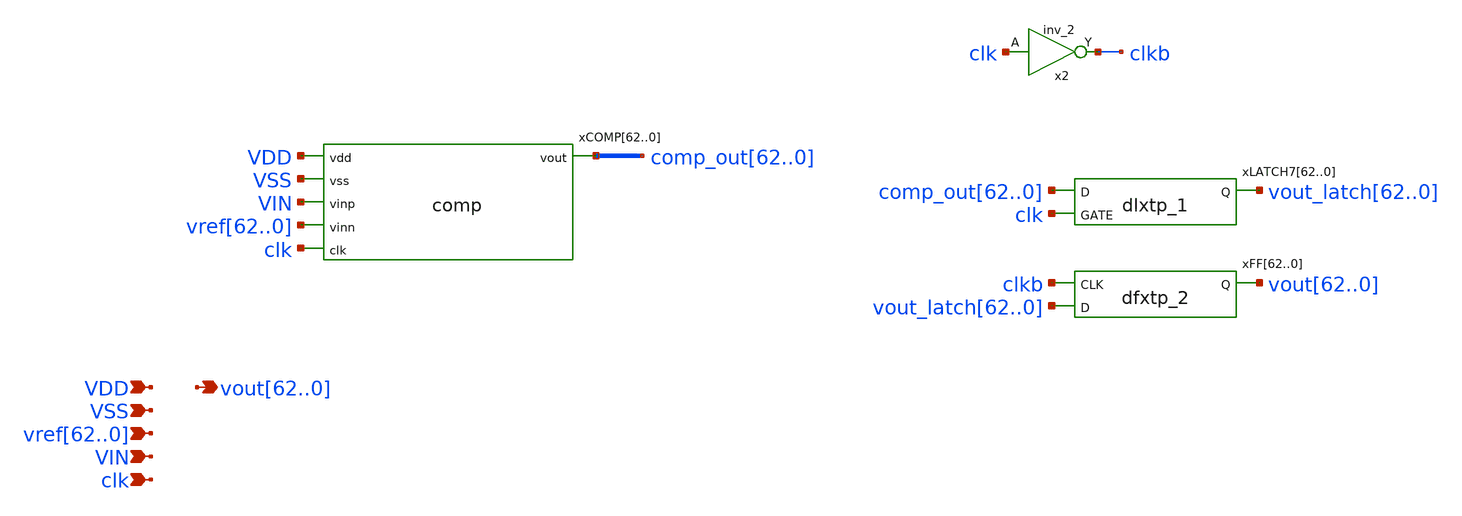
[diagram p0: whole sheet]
** sch_path: schematics/comp_top.sch
**.subckt comp_top
*+ vout62,vout61,vout60,vout59,vout58,vout57,vout56,vout55,vout54,vout53,vout52,vout51,vout50,vout49,vout48,vout47,vout46,vout45,vout44,vout43,vout42,vout41,vout40,vout39,vout38,vout37,vout36,vout35,vout34,vout33,vout32,vout31,vout30,vout29,vout28,vout27,vout26,vout25,vout24,vout23,vout22,vout21,vout20,vout19,vout18,vout17,vout16,vout15,vout14,vout13,vout12,vout11,vout10,vout9,vout8,vout7,vout6,vout5,vout4,vout3,vout2,vout1,vout0 VDD VSS
*+ vref62,vref61,vref60,vref59,vref58,vref57,vref56,vref55,vref54,vref53,vref52,vref51,vref50,vref49,vref48,vref47,vref46,vref45,vref44,vref43,vref42,vref41,vref40,vref39,vref38,vref37,vref36,vref35,vref34,vref33,vref32,vref31,vref30,vref29,vref28,vref27,vref26,vref25,vref24,vref23,vref22,vref21,vref20,vref19,vref18,vref17,vref16,vref15,vref14,vref13,vref12,vref11,vref10,vref9,vref8,vref7,vref6,vref5,vref4,vref3,vref2,vref1,vref0 VIN clk
*.opin
*+ vout62,vout61,vout60,vout59,vout58,vout57,vout56,vout55,vout54,vout53,vout52,vout51,vout50,vout49,vout48,vout47,vout46,vout45,vout44,vout43,vout42,vout41,vout40,vout39,vout38,vout37,vout36,vout35,vout34,vout33,vout32,vout31,vout30,vout29,vout28,vout27,vout26,vout25,vout24,vout23,vout22,vout21,vout20,vout19,vout18,vout17,vout16,vout15,vout14,vout13,vout12,vout11,vout10,vout9,vout8,vout7,vout6,vout5,vout4,vout3,vout2,vout1,vout0
*.ipin VDD
*.ipin VSS
*.ipin
*+ vref62,vref61,vref60,vref59,vref58,vref57,vref56,vref55,vref54,vref53,vref52,vref51,vref50,vref49,vref48,vref47,vref46,vref45,vref44,vref43,vref42,vref41,vref40,vref39,vref38,vref37,vref36,vref35,vref34,vref33,vref32,vref31,vref30,vref29,vref28,vref27,vref26,vref25,vref24,vref23,vref22,vref21,vref20,vref19,vref18,vref17,vref16,vref15,vref14,vref13,vref12,vref11,vref10,vref9,vref8,vref7,vref6,vref5,vref4,vref3,vref2,vref1,vref0
*.ipin VIN
*.ipin clk
xCOMP62 comp_out62 VDD VSS VIN vref62 clk comp
xCOMP61 comp_out61 VDD VSS VIN vref61 clk comp
xCOMP60 comp_out60 VDD VSS VIN vref60 clk comp
xCOMP59 comp_out59 VDD VSS VIN vref59 clk comp
xCOMP58 comp_out58 VDD VSS VIN vref58 clk comp
xCOMP57 comp_out57 VDD VSS VIN vref57 clk comp
xCOMP56 comp_out56 VDD VSS VIN vref56 clk comp
xCOMP55 comp_out55 VDD VSS VIN vref55 clk comp
xCOMP54 comp_out54 VDD VSS VIN vref54 clk comp
xCOMP53 comp_out53 VDD VSS VIN vref53 clk comp
xCOMP52 comp_out52 VDD VSS VIN vref52 clk comp
xCOMP51 comp_out51 VDD VSS VIN vref51 clk comp
xCOMP50 comp_out50 VDD VSS VIN vref50 clk comp
xCOMP49 comp_out49 VDD VSS VIN vref49 clk comp
xCOMP48 comp_out48 VDD VSS VIN vref48 clk comp
xCOMP47 comp_out47 VDD VSS VIN vref47 clk comp
xCOMP46 comp_out46 VDD VSS VIN vref46 clk comp
xCOMP45 comp_out45 VDD VSS VIN vref45 clk comp
xCOMP44 comp_out44 VDD VSS VIN vref44 clk comp
xCOMP43 comp_out43 VDD VSS VIN vref43 clk comp
xCOMP42 comp_out42 VDD VSS VIN vref42 clk comp
xCOMP41 comp_out41 VDD VSS VIN vref41 clk comp
xCOMP40 comp_out40 VDD VSS VIN vref40 clk comp
xCOMP39 comp_out39 VDD VSS VIN vref39 clk comp
xCOMP38 comp_out38 VDD VSS VIN vref38 clk comp
xCOMP37 comp_out37 VDD VSS VIN vref37 clk comp
xCOMP36 comp_out36 VDD VSS VIN vref36 clk comp
xCOMP35 comp_out35 VDD VSS VIN vref35 clk comp
xCOMP34 comp_out34 VDD VSS VIN vref34 clk comp
xCOMP33 comp_out33 VDD VSS VIN vref33 clk comp
xCOMP32 comp_out32 VDD VSS VIN vref32 clk comp
xCOMP31 comp_out31 VDD VSS VIN vref31 clk comp
xCOMP30 comp_out30 VDD VSS VIN vref30 clk comp
xCOMP29 comp_out29 VDD VSS VIN vref29 clk comp
xCOMP28 comp_out28 VDD VSS VIN vref28 clk comp
xCOMP27 comp_out27 VDD VSS VIN vref27 clk comp
xCOMP26 comp_out26 VDD VSS VIN vref26 clk comp
xCOMP25 comp_out25 VDD VSS VIN vref25 clk comp
xCOMP24 comp_out24 VDD VSS VIN vref24 clk comp
xCOMP23 comp_out23 VDD VSS VIN vref23 clk comp
xCOMP22 comp_out22 VDD VSS VIN vref22 clk comp
xCOMP21 comp_out21 VDD VSS VIN vref21 clk comp
xCOMP20 comp_out20 VDD VSS VIN vref20 clk comp
xCOMP19 comp_out19 VDD VSS VIN vref19 clk comp
xCOMP18 comp_out18 VDD VSS VIN vref18 clk comp
xCOMP17 comp_out17 VDD VSS VIN vref17 clk comp
xCOMP16 comp_out16 VDD VSS VIN vref16 clk comp
xCOMP15 comp_out15 VDD VSS VIN vref15 clk comp
xCOMP14 comp_out14 VDD VSS VIN vref14 clk comp
xCOMP13 comp_out13 VDD VSS VIN vref13 clk comp
xCOMP12 comp_out12 VDD VSS VIN vref12 clk comp
xCOMP11 comp_out11 VDD VSS VIN vref11 clk comp
xCOMP10 comp_out10 VDD VSS VIN vref10 clk comp
xCOMP9 comp_out9 VDD VSS VIN vref9 clk comp
xCOMP8 comp_out8 VDD VSS VIN vref8 clk comp
xCOMP7 comp_out7 VDD VSS VIN vref7 clk comp
xCOMP6 comp_out6 VDD VSS VIN vref6 clk comp
xCOMP5 comp_out5 VDD VSS VIN vref5 clk comp
xCOMP4 comp_out4 VDD VSS VIN vref4 clk comp
xCOMP3 comp_out3 VDD VSS VIN vref3 clk comp
xCOMP2 comp_out2 VDD VSS VIN vref2 clk comp
xCOMP1 comp_out1 VDD VSS VIN vref1 clk comp
xCOMP0 comp_out0 VDD VSS VIN vref0 clk comp
x2 clk vss vss vdd vdd clkb sky130_fd_sc_hd__inv_2
xLATCH762 comp_out62 clk vss vss vdd vdd vout_latch62 sky130_fd_sc_hd__dlxtp_1
xLATCH761 comp_out61 clk vss vss vdd vdd vout_latch61 sky130_fd_sc_hd__dlxtp_1
xLATCH760 comp_out60 clk vss vss vdd vdd vout_latch60 sky130_fd_sc_hd__dlxtp_1
xLATCH759 comp_out59 clk vss vss vdd vdd vout_latch59 sky130_fd_sc_hd__dlxtp_1
xLATCH758 comp_out58 clk vss vss vdd vdd vout_latch58 sky130_fd_sc_hd__dlxtp_1
xLATCH757 comp_out57 clk vss vss vdd vdd vout_latch57 sky130_fd_sc_hd__dlxtp_1
xLATCH756 comp_out56 clk vss vss vdd vdd vout_latch56 sky130_fd_sc_hd__dlxtp_1
xLATCH755 comp_out55 clk vss vss vdd vdd vout_latch55 sky130_fd_sc_hd__dlxtp_1
xLATCH754 comp_out54 clk vss vss vdd vdd vout_latch54 sky130_fd_sc_hd__dlxtp_1
xLATCH753 comp_out53 clk vss vss vdd vdd vout_latch53 sky130_fd_sc_hd__dlxtp_1
xLATCH752 comp_out52 clk vss vss vdd vdd vout_latch52 sky130_fd_sc_hd__dlxtp_1
xLATCH751 comp_out51 clk vss vss vdd vdd vout_latch51 sky130_fd_sc_hd__dlxtp_1
xLATCH750 comp_out50 clk vss vss vdd vdd vout_latch50 sky130_fd_sc_hd__dlxtp_1
xLATCH749 comp_out49 clk vss vss vdd vdd vout_latch49 sky130_fd_sc_hd__dlxtp_1
xLATCH748 comp_out48 clk vss vss vdd vdd vout_latch48 sky130_fd_sc_hd__dlxtp_1
xLATCH747 comp_out47 clk vss vss vdd vdd vout_latch47 sky130_fd_sc_hd__dlxtp_1
xLATCH746 comp_out46 clk vss vss vdd vdd vout_latch46 sky130_fd_sc_hd__dlxtp_1
xLATCH745 comp_out45 clk vss vss vdd vdd vout_latch45 sky130_fd_sc_hd__dlxtp_1
xLATCH744 comp_out44 clk vss vss vdd vdd vout_latch44 sky130_fd_sc_hd__dlxtp_1
xLATCH743 comp_out43 clk vss vss vdd vdd vout_latch43 sky130_fd_sc_hd__dlxtp_1
xLATCH742 comp_out42 clk vss vss vdd vdd vout_latch42 sky130_fd_sc_hd__dlxtp_1
xLATCH741 comp_out41 clk vss vss vdd vdd vout_latch41 sky130_fd_sc_hd__dlxtp_1
xLATCH740 comp_out40 clk vss vss vdd vdd vout_latch40 sky130_fd_sc_hd__dlxtp_1
xLATCH739 comp_out39 clk vss vss vdd vdd vout_latch39 sky130_fd_sc_hd__dlxtp_1
xLATCH738 comp_out38 clk vss vss vdd vdd vout_latch38 sky130_fd_sc_hd__dlxtp_1
xLATCH737 comp_out37 clk vss vss vdd vdd vout_latch37 sky130_fd_sc_hd__dlxtp_1
xLATCH736 comp_out36 clk vss vss vdd vdd vout_latch36 sky130_fd_sc_hd__dlxtp_1
xLATCH735 comp_out35 clk vss vss vdd vdd vout_latch35 sky130_fd_sc_hd__dlxtp_1
xLATCH734 comp_out34 clk vss vss vdd vdd vout_latch34 sky130_fd_sc_hd__dlxtp_1
xLATCH733 comp_out33 clk vss vss vdd vdd vout_latch33 sky130_fd_sc_hd__dlxtp_1
xLATCH732 comp_out32 clk vss vss vdd vdd vout_latch32 sky130_fd_sc_hd__dlxtp_1
xLATCH731 comp_out31 clk vss vss vdd vdd vout_latch31 sky130_fd_sc_hd__dlxtp_1
xLATCH730 comp_out30 clk vss vss vdd vdd vout_latch30 sky130_fd_sc_hd__dlxtp_1
xLATCH729 comp_out29 clk vss vss vdd vdd vout_latch29 sky130_fd_sc_hd__dlxtp_1
xLATCH728 comp_out28 clk vss vss vdd vdd vout_latch28 sky130_fd_sc_hd__dlxtp_1
xLATCH727 comp_out27 clk vss vss vdd vdd vout_latch27 sky130_fd_sc_hd__dlxtp_1
xLATCH726 comp_out26 clk vss vss vdd vdd vout_latch26 sky130_fd_sc_hd__dlxtp_1
xLATCH725 comp_out25 clk vss vss vdd vdd vout_latch25 sky130_fd_sc_hd__dlxtp_1
xLATCH724 comp_out24 clk vss vss vdd vdd vout_latch24 sky130_fd_sc_hd__dlxtp_1
xLATCH723 comp_out23 clk vss vss vdd vdd vout_latch23 sky130_fd_sc_hd__dlxtp_1
xLATCH722 comp_out22 clk vss vss vdd vdd vout_latch22 sky130_fd_sc_hd__dlxtp_1
xLATCH721 comp_out21 clk vss vss vdd vdd vout_latch21 sky130_fd_sc_hd__dlxtp_1
xLATCH720 comp_out20 clk vss vss vdd vdd vout_latch20 sky130_fd_sc_hd__dlxtp_1
xLATCH719 comp_out19 clk vss vss vdd vdd vout_latch19 sky130_fd_sc_hd__dlxtp_1
xLATCH718 comp_out18 clk vss vss vdd vdd vout_latch18 sky130_fd_sc_hd__dlxtp_1
xLATCH717 comp_out17 clk vss vss vdd vdd vout_latch17 sky130_fd_sc_hd__dlxtp_1
xLATCH716 comp_out16 clk vss vss vdd vdd vout_latch16 sky130_fd_sc_hd__dlxtp_1
xLATCH715 comp_out15 clk vss vss vdd vdd vout_latch15 sky130_fd_sc_hd__dlxtp_1
xLATCH714 comp_out14 clk vss vss vdd vdd vout_latch14 sky130_fd_sc_hd__dlxtp_1
xLATCH713 comp_out13 clk vss vss vdd vdd vout_latch13 sky130_fd_sc_hd__dlxtp_1
xLATCH712 comp_out12 clk vss vss vdd vdd vout_latch12 sky130_fd_sc_hd__dlxtp_1
xLATCH711 comp_out11 clk vss vss vdd vdd vout_latch11 sky130_fd_sc_hd__dlxtp_1
xLATCH710 comp_out10 clk vss vss vdd vdd vout_latch10 sky130_fd_sc_hd__dlxtp_1
xLATCH79 comp_out9 clk vss vss vdd vdd vout_latch9 sky130_fd_sc_hd__dlxtp_1
xLATCH78 comp_out8 clk vss vss vdd vdd vout_latch8 sky130_fd_sc_hd__dlxtp_1
xLATCH77 comp_out7 clk vss vss vdd vdd vout_latch7 sky130_fd_sc_hd__dlxtp_1
xLATCH76 comp_out6 clk vss vss vdd vdd vout_latch6 sky130_fd_sc_hd__dlxtp_1
xLATCH75 comp_out5 clk vss vss vdd vdd vout_latch5 sky130_fd_sc_hd__dlxtp_1
xLATCH74 comp_out4 clk vss vss vdd vdd vout_latch4 sky130_fd_sc_hd__dlxtp_1
xLATCH73 comp_out3 clk vss vss vdd vdd vout_latch3 sky130_fd_sc_hd__dlxtp_1
xLATCH72 comp_out2 clk vss vss vdd vdd vout_latch2 sky130_fd_sc_hd__dlxtp_1
xLATCH71 comp_out1 clk vss vss vdd vdd vout_latch1 sky130_fd_sc_hd__dlxtp_1
xLATCH70 comp_out0 clk vss vss vdd vdd vout_latch0 sky130_fd_sc_hd__dlxtp_1
xFF62 clkb vout_latch62 vss vss vdd vdd vout62 sky130_fd_sc_hd__dfxtp_2
xFF61 clkb vout_latch61 vss vss vdd vdd vout61 sky130_fd_sc_hd__dfxtp_2
xFF60 clkb vout_latch60 vss vss vdd vdd vout60 sky130_fd_sc_hd__dfxtp_2
xFF59 clkb vout_latch59 vss vss vdd vdd vout59 sky130_fd_sc_hd__dfxtp_2
xFF58 clkb vout_latch58 vss vss vdd vdd vout58 sky130_fd_sc_hd__dfxtp_2
xFF57 clkb vout_latch57 vss vss vdd vdd vout57 sky130_fd_sc_hd__dfxtp_2
xFF56 clkb vout_latch56 vss vss vdd vdd vout56 sky130_fd_sc_hd__dfxtp_2
xFF55 clkb vout_latch55 vss vss vdd vdd vout55 sky130_fd_sc_hd__dfxtp_2
xFF54 clkb vout_latch54 vss vss vdd vdd vout54 sky130_fd_sc_hd__dfxtp_2
xFF53 clkb vout_latch53 vss vss vdd vdd vout53 sky130_fd_sc_hd__dfxtp_2
xFF52 clkb vout_latch52 vss vss vdd vdd vout52 sky130_fd_sc_hd__dfxtp_2
xFF51 clkb vout_latch51 vss vss vdd vdd vout51 sky130_fd_sc_hd__dfxtp_2
xFF50 clkb vout_latch50 vss vss vdd vdd vout50 sky130_fd_sc_hd__dfxtp_2
xFF49 clkb vout_latch49 vss vss vdd vdd vout49 sky130_fd_sc_hd__dfxtp_2
xFF48 clkb vout_latch48 vss vss vdd vdd vout48 sky130_fd_sc_hd__dfxtp_2
xFF47 clkb vout_latch47 vss vss vdd vdd vout47 sky130_fd_sc_hd__dfxtp_2
xFF46 clkb vout_latch46 vss vss vdd vdd vout46 sky130_fd_sc_hd__dfxtp_2
xFF45 clkb vout_latch45 vss vss vdd vdd vout45 sky130_fd_sc_hd__dfxtp_2
xFF44 clkb vout_latch44 vss vss vdd vdd vout44 sky130_fd_sc_hd__dfxtp_2
xFF43 clkb vout_latch43 vss vss vdd vdd vout43 sky130_fd_sc_hd__dfxtp_2
xFF42 clkb vout_latch42 vss vss vdd vdd vout42 sky130_fd_sc_hd__dfxtp_2
xFF41 clkb vout_latch41 vss vss vdd vdd vout41 sky130_fd_sc_hd__dfxtp_2
xFF40 clkb vout_latch40 vss vss vdd vdd vout40 sky130_fd_sc_hd__dfxtp_2
xFF39 clkb vout_latch39 vss vss vdd vdd vout39 sky130_fd_sc_hd__dfxtp_2
xFF38 clkb vout_latch38 vss vss vdd vdd vout38 sky130_fd_sc_hd__dfxtp_2
xFF37 clkb vout_latch37 vss vss vdd vdd vout37 sky130_fd_sc_hd__dfxtp_2
xFF36 clkb vout_latch36 vss vss vdd vdd vout36 sky130_fd_sc_hd__dfxtp_2
xFF35 clkb vout_latch35 vss vss vdd vdd vout35 sky130_fd_sc_hd__dfxtp_2
xFF34 clkb vout_latch34 vss vss vdd vdd vout34 sky130_fd_sc_hd__dfxtp_2
xFF33 clkb vout_latch33 vss vss vdd vdd vout33 sky130_fd_sc_hd__dfxtp_2
xFF32 clkb vout_latch32 vss vss vdd vdd vout32 sky130_fd_sc_hd__dfxtp_2
xFF31 clkb vout_latch31 vss vss vdd vdd vout31 sky130_fd_sc_hd__dfxtp_2
xFF30 clkb vout_latch30 vss vss vdd vdd vout30 sky130_fd_sc_hd__dfxtp_2
xFF29 clkb vout_latch29 vss vss vdd vdd vout29 sky130_fd_sc_hd__dfxtp_2
xFF28 clkb vout_latch28 vss vss vdd vdd vout28 sky130_fd_sc_hd__dfxtp_2
xFF27 clkb vout_latch27 vss vss vdd vdd vout27 sky130_fd_sc_hd__dfxtp_2
xFF26 clkb vout_latch26 vss vss vdd vdd vout26 sky130_fd_sc_hd__dfxtp_2
xFF25 clkb vout_latch25 vss vss vdd vdd vout25 sky130_fd_sc_hd__dfxtp_2
xFF24 clkb vout_latch24 vss vss vdd vdd vout24 sky130_fd_sc_hd__dfxtp_2
xFF23 clkb vout_latch23 vss vss vdd vdd vout23 sky130_fd_sc_hd__dfxtp_2
xFF22 clkb vout_latch22 vss vss vdd vdd vout22 sky130_fd_sc_hd__dfxtp_2
xFF21 clkb vout_latch21 vss vss vdd vdd vout21 sky130_fd_sc_hd__dfxtp_2
xFF20 clkb vout_latch20 vss vss vdd vdd vout20 sky130_fd_sc_hd__dfxtp_2
xFF19 clkb vout_latch19 vss vss vdd vdd vout19 sky130_fd_sc_hd__dfxtp_2
xFF18 clkb vout_latch18 vss vss vdd vdd vout18 sky130_fd_sc_hd__dfxtp_2
xFF17 clkb vout_latch17 vss vss vdd vdd vout17 sky130_fd_sc_hd__dfxtp_2
xFF16 clkb vout_latch16 vss vss vdd vdd vout16 sky130_fd_sc_hd__dfxtp_2
xFF15 clkb vout_latch15 vss vss vdd vdd vout15 sky130_fd_sc_hd__dfxtp_2
xFF14 clkb vout_latch14 vss vss vdd vdd vout14 sky130_fd_sc_hd__dfxtp_2
xFF13 clkb vout_latch13 vss vss vdd vdd vout13 sky130_fd_sc_hd__dfxtp_2
xFF12 clkb vout_latch12 vss vss vdd vdd vout12 sky130_fd_sc_hd__dfxtp_2
xFF11 clkb vout_latch11 vss vss vdd vdd vout11 sky130_fd_sc_hd__dfxtp_2
xFF10 clkb vout_latch10 vss vss vdd vdd vout10 sky130_fd_sc_hd__dfxtp_2
xFF9 clkb vout_latch9 vss vss vdd vdd vout9 sky130_fd_sc_hd__dfxtp_2
xFF8 clkb vout_latch8 vss vss vdd vdd vout8 sky130_fd_sc_hd__dfxtp_2
xFF7 clkb vout_latch7 vss vss vdd vdd vout7 sky130_fd_sc_hd__dfxtp_2
xFF6 clkb vout_latch6 vss vss vdd vdd vout6 sky130_fd_sc_hd__dfxtp_2
xFF5 clkb vout_latch5 vss vss vdd vdd vout5 sky130_fd_sc_hd__dfxtp_2
xFF4 clkb vout_latch4 vss vss vdd vdd vout4 sky130_fd_sc_hd__dfxtp_2
xFF3 clkb vout_latch3 vss vss vdd vdd vout3 sky130_fd_sc_hd__dfxtp_2
xFF2 clkb vout_latch2 vss vss vdd vdd vout2 sky130_fd_sc_hd__dfxtp_2
xFF1 clkb vout_latch1 vss vss vdd vdd vout1 sky130_fd_sc_hd__dfxtp_2
xFF0 clkb vout_latch0 vss vss vdd vdd vout0 sky130_fd_sc_hd__dfxtp_2
**.ends

* expanding   symbol:  schematics/comp.sym # of pins=6
** sym_path: schematics/comp.sym
** sch_path: schematics/comp.sch
.subckt comp vout vdd vss vinp vinn clk
*.ipin vdd
*.opin vout
*.ipin vss
*.ipin vinp
*.ipin vinn
*.ipin clk
XM6 net1 clk vss vss sky130_fd_pr__nfet_01v8 L=0.15 W=1 nf=1 ad='int((1 + 1)/2) * 1 / 1 * 0.29' as='int((1 + 2)/2) * 1 / 1 * 0.29'
+ pd='2*int((1 + 1)/2) * (1 / 1 + 0.29)' ps='2*int((1 + 2)/2) * (1 / 1 + 0.29)' nrd='0.29 / 1 ' nrs='0.29 / 1 '
+ sa=0 sb=0 sd=0 mult=1 m=1
XM10 voutn voutp vdd vdd sky130_fd_pr__pfet_01v8 L=0.15 W=1 nf=1 ad='int((1 + 1)/2) * 1 / 1 * 0.29' as='int((1 + 2)/2) * 1 / 1 * 0.29'
+ pd='2*int((1 + 1)/2) * (1 / 1 + 0.29)' ps='2*int((1 + 2)/2) * (1 / 1 + 0.29)' nrd='0.29 / 1 ' nrs='0.29 / 1 '
+ sa=0 sb=0 sd=0 mult=1 m=1
xBUFF voutp vss vss vdd vdd voutp_buff sky130_fd_sc_hd__buf_6
xBUFF1 voutn vss vss vdd vdd voutn_buff sky130_fd_sc_hd__buf_6
I0 pa_m1_s vss 10u
XM11 v_m1_d voutp_buff pa_m1_s vss sky130_fd_pr__nfet_01v8 L=0.15 W=50 nf=1 ad='int((1 + 1)/2) * 50 / 1 * 0.29'
+ as='int((1 + 2)/2) * 50 / 1 * 0.29' pd='2*int((1 + 1)/2) * (50 / 1 + 0.29)' ps='2*int((1 + 2)/2) * (50 / 1 + 0.29)'
+ nrd='0.29 / 50 ' nrs='0.29 / 50 ' sa=0 sb=0 sd=0 mult=1 m=1
XM12 vout voutn_buff pa_m1_s vss sky130_fd_pr__nfet_01v8 L=0.15 W=50 nf=1 ad='int((1 + 1)/2) * 50 / 1 * 0.29'
+ as='int((1 + 2)/2) * 50 / 1 * 0.29' pd='2*int((1 + 1)/2) * (50 / 1 + 0.29)' ps='2*int((1 + 2)/2) * (50 / 1 + 0.29)'
+ nrd='0.29 / 50 ' nrs='0.29 / 50 ' sa=0 sb=0 sd=0 mult=1 m=1
XM13 v_m1_d v_m1_d vdd vdd sky130_fd_pr__pfet_01v8 L=0.5 W=2 nf=1 ad='int((1 + 1)/2) * 2 / 1 * 0.29'
+ as='int((1 + 2)/2) * 2 / 1 * 0.29' pd='2*int((1 + 1)/2) * (2 / 1 + 0.29)' ps='2*int((1 + 2)/2) * (2 / 1 + 0.29)'
+ nrd='0.29 / 2 ' nrs='0.29 / 2 ' sa=0 sb=0 sd=0 mult=1 m=1
XM14 vout v_m1_d vdd vdd sky130_fd_pr__pfet_01v8 L=0.5 W=2 nf=1 ad='int((1 + 1)/2) * 2 / 1 * 0.29' as='int((1 + 2)/2) * 2 / 1 * 0.29'
+ pd='2*int((1 + 1)/2) * (2 / 1 + 0.29)' ps='2*int((1 + 2)/2) * (2 / 1 + 0.29)' nrd='0.29 / 2 ' nrs='0.29 / 2 '
+ sa=0 sb=0 sd=0 mult=1 m=1
XM1 vinp_d vinp net1 vss sky130_fd_pr__nfet_01v8 L=0.15 W=20 nf=1 ad='int((1 + 1)/2) * 20 / 1 * 0.29'
+ as='int((1 + 2)/2) * 20 / 1 * 0.29' pd='2*int((1 + 1)/2) * (20 / 1 + 0.29)' ps='2*int((1 + 2)/2) * (20 / 1 + 0.29)'
+ nrd='0.29 / 20 ' nrs='0.29 / 20 ' sa=0 sb=0 sd=0 mult=1 m=1
XM2 vinn_d vinn net1 vss sky130_fd_pr__nfet_01v8 L=0.15 W=20 nf=1 ad='int((1 + 1)/2) * 20 / 1 * 0.29'
+ as='int((1 + 2)/2) * 20 / 1 * 0.29' pd='2*int((1 + 1)/2) * (20 / 1 + 0.29)' ps='2*int((1 + 2)/2) * (20 / 1 + 0.29)'
+ nrd='0.29 / 20 ' nrs='0.29 / 20 ' sa=0 sb=0 sd=0 mult=1 m=1
XM3 voutn voutp vinp_d vss sky130_fd_pr__nfet_01v8 L=0.15 W=1 nf=1 ad='int((1 + 1)/2) * 1 / 1 * 0.29'
+ as='int((1 + 2)/2) * 1 / 1 * 0.29' pd='2*int((1 + 1)/2) * (1 / 1 + 0.29)' ps='2*int((1 + 2)/2) * (1 / 1 + 0.29)'
+ nrd='0.29 / 1 ' nrs='0.29 / 1 ' sa=0 sb=0 sd=0 mult=1 m=1
XM4 voutp voutn vinn_d vss sky130_fd_pr__nfet_01v8 L=0.15 W=1 nf=1 ad='int((1 + 1)/2) * 1 / 1 * 0.29'
+ as='int((1 + 2)/2) * 1 / 1 * 0.29' pd='2*int((1 + 1)/2) * (1 / 1 + 0.29)' ps='2*int((1 + 2)/2) * (1 / 1 + 0.29)'
+ nrd='0.29 / 1 ' nrs='0.29 / 1 ' sa=0 sb=0 sd=0 mult=1 m=1
XM5 voutp voutn vdd vdd sky130_fd_pr__pfet_01v8 L=0.15 W=1 nf=1 ad='int((1 + 1)/2) * 1 / 1 * 0.29' as='int((1 + 2)/2) * 1 / 1 * 0.29'
+ pd='2*int((1 + 1)/2) * (1 / 1 + 0.29)' ps='2*int((1 + 2)/2) * (1 / 1 + 0.29)' nrd='0.29 / 1 ' nrs='0.29 / 1 '
+ sa=0 sb=0 sd=0 mult=1 m=1
XM7 voutp clk vdd vdd sky130_fd_pr__pfet_01v8 L=0.15 W=1 nf=1 ad='int((1 + 1)/2) * 1 / 1 * 0.29' as='int((1 + 2)/2) * 1 / 1 * 0.29'
+ pd='2*int((1 + 1)/2) * (1 / 1 + 0.29)' ps='2*int((1 + 2)/2) * (1 / 1 + 0.29)' nrd='0.29 / 1 ' nrs='0.29 / 1 '
+ sa=0 sb=0 sd=0 mult=1 m=1
XM8 voutn clk vdd vdd sky130_fd_pr__pfet_01v8 L=0.15 W=1 nf=1 ad='int((1 + 1)/2) * 1 / 1 * 0.29' as='int((1 + 2)/2) * 1 / 1 * 0.29'
+ pd='2*int((1 + 1)/2) * (1 / 1 + 0.29)' ps='2*int((1 + 2)/2) * (1 / 1 + 0.29)' nrd='0.29 / 1 ' nrs='0.29 / 1 '
+ sa=0 sb=0 sd=0 mult=1 m=1
.ends

.end
